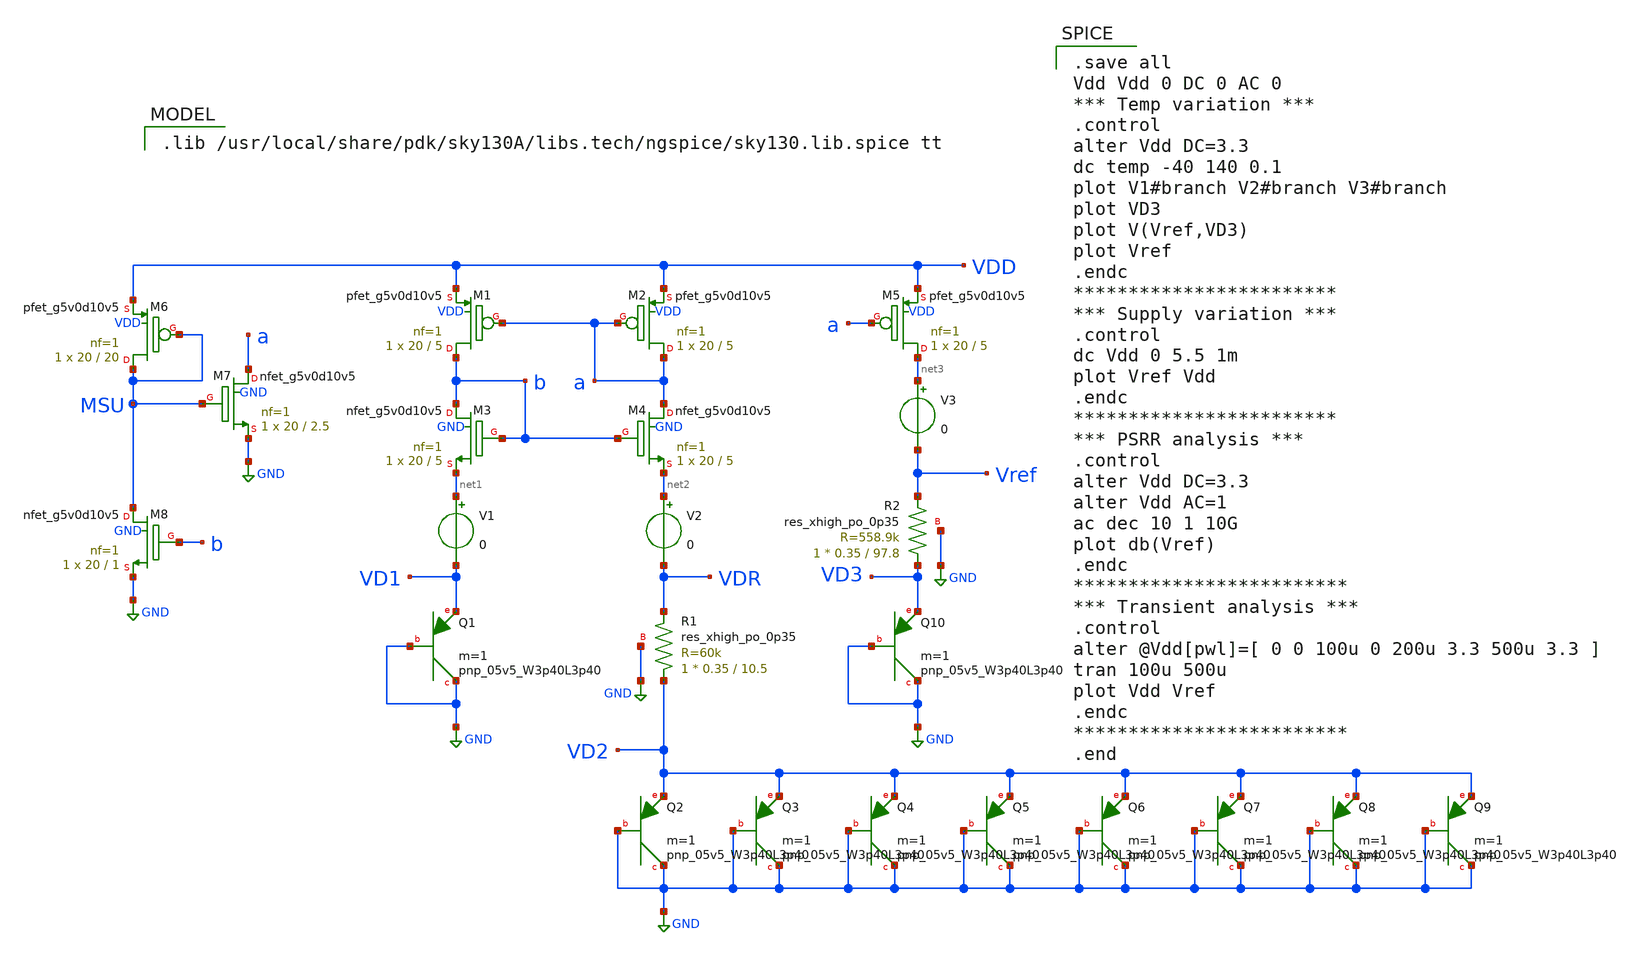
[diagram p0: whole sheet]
** sch_path: 2_BGR_nocas_60k_3p4pnp.sch
**.subckt 2_BGR_nocas_60k_3p4pnp
V1 net1 VD1 0
V2 net2 VDR 0
V3 net3 Vref 0
XR1 VD2 VDR GND sky130_fd_pr__res_xhigh_po_0p35 L=10.5 mult=1 m=1
XR2 VD3 Vref GND sky130_fd_pr__res_xhigh_po_0p35 L=97.8 mult=1 m=1
XM1 b a VDD VDD sky130_fd_pr__pfet_g5v0d10v5 L=5 W=20 nf=1 ad='int((nf+1)/2) * W/nf * 0.29' as='int((nf+2)/2) * W/nf * 0.29'
+ pd='2*int((nf+1)/2) * (W/nf + 0.29)' ps='2*int((nf+2)/2) * (W/nf + 0.29)' nrd='0.29 / W' nrs='0.29 / W'
+ sa=0 sb=0 sd=0 mult=1 m=1
XM2 a a VDD VDD sky130_fd_pr__pfet_g5v0d10v5 L=5 W=20 nf=1 ad='int((nf+1)/2) * W/nf * 0.29' as='int((nf+2)/2) * W/nf * 0.29'
+ pd='2*int((nf+1)/2) * (W/nf + 0.29)' ps='2*int((nf+2)/2) * (W/nf + 0.29)' nrd='0.29 / W' nrs='0.29 / W'
+ sa=0 sb=0 sd=0 mult=1 m=1
XM3 b b net1 GND sky130_fd_pr__nfet_g5v0d10v5 L=5 W=20 nf=1 ad='int((nf+1)/2) * W/nf * 0.29' as='int((nf+2)/2) * W/nf * 0.29'
+ pd='2*int((nf+1)/2) * (W/nf + 0.29)' ps='2*int((nf+2)/2) * (W/nf + 0.29)' nrd='0.29 / W' nrs='0.29 / W'
+ sa=0 sb=0 sd=0 mult=1 m=1
XM4 a b net2 GND sky130_fd_pr__nfet_g5v0d10v5 L=5 W=20 nf=1 ad='int((nf+1)/2) * W/nf * 0.29' as='int((nf+2)/2) * W/nf * 0.29'
+ pd='2*int((nf+1)/2) * (W/nf + 0.29)' ps='2*int((nf+2)/2) * (W/nf + 0.29)' nrd='0.29 / W' nrs='0.29 / W'
+ sa=0 sb=0 sd=0 mult=1 m=1
XM5 net3 a VDD VDD sky130_fd_pr__pfet_g5v0d10v5 L=5 W=20 nf=1 ad='int((nf+1)/2) * W/nf * 0.29' as='int((nf+2)/2) * W/nf * 0.29'
+ pd='2*int((nf+1)/2) * (W/nf + 0.29)' ps='2*int((nf+2)/2) * (W/nf + 0.29)' nrd='0.29 / W' nrs='0.29 / W'
+ sa=0 sb=0 sd=0 mult=1 m=1
XM8 MSU b GND GND sky130_fd_pr__nfet_g5v0d10v5 L=1 W=20 nf=1 ad='int((nf+1)/2) * W/nf * 0.29' as='int((nf+2)/2) * W/nf * 0.29'
+ pd='2*int((nf+1)/2) * (W/nf + 0.29)' ps='2*int((nf+2)/2) * (W/nf + 0.29)' nrd='0.29 / W' nrs='0.29 / W'
+ sa=0 sb=0 sd=0 mult=1 m=1
XM7 a MSU GND GND sky130_fd_pr__nfet_g5v0d10v5 L=2.5 W=20 nf=1 ad='int((nf+1)/2) * W/nf * 0.29' as='int((nf+2)/2) * W/nf * 0.29'
+ pd='2*int((nf+1)/2) * (W/nf + 0.29)' ps='2*int((nf+2)/2) * (W/nf + 0.29)' nrd='0.29 / W' nrs='0.29 / W'
+ sa=0 sb=0 sd=0 mult=1 m=1
XQ1 GND GND VD1 sky130_fd_pr__pnp_05v5_W3p40L3p40 m=1
XQ2 GND GND VD2 sky130_fd_pr__pnp_05v5_W3p40L3p40 m=1
XQ3 GND GND VD2 sky130_fd_pr__pnp_05v5_W3p40L3p40 m=1
XQ4 GND GND VD2 sky130_fd_pr__pnp_05v5_W3p40L3p40 m=1
XQ5 GND GND VD2 sky130_fd_pr__pnp_05v5_W3p40L3p40 m=1
XQ6 GND GND VD2 sky130_fd_pr__pnp_05v5_W3p40L3p40 m=1
XQ7 GND GND VD2 sky130_fd_pr__pnp_05v5_W3p40L3p40 m=1
XQ8 GND GND VD2 sky130_fd_pr__pnp_05v5_W3p40L3p40 m=1
XQ9 GND GND VD2 sky130_fd_pr__pnp_05v5_W3p40L3p40 m=1
XQ10 GND GND VD3 sky130_fd_pr__pnp_05v5_W3p40L3p40 m=1
XM6 MSU MSU VDD VDD sky130_fd_pr__pfet_g5v0d10v5 L=20 W=20 nf=1 ad='int((nf+1)/2) * W/nf * 0.29' as='int((nf+2)/2) * W/nf * 0.29'
+ pd='2*int((nf+1)/2) * (W/nf + 0.29)' ps='2*int((nf+2)/2) * (W/nf + 0.29)' nrd='0.29 / W' nrs='0.29 / W'
+ sa=0 sb=0 sd=0 mult=1 m=1
**** begin user architecture code

.lib /usr/local/share/pdk/sky130A/libs.tech/ngspice/sky130.lib.spice tt


.save all
Vdd Vdd 0 DC 0 AC 0
*** Temp variation ***
.control
alter Vdd DC=3.3
dc temp -40 140 0.1
plot V1#branch V2#branch V3#branch
plot VD3
plot V(Vref,VD3)
plot Vref
.endc
************************
*** Supply variation ***
.control
dc Vdd 0 5.5 1m
plot Vref Vdd
.endc
************************
*** PSRR analysis ***
.control
alter Vdd DC=3.3
alter Vdd AC=1
ac dec 10 1 10G
plot db(Vref)
.endc
*************************
*** Transient analysis ***
.control
alter @Vdd[pwl]=[ 0 0 100u 0 200u 3.3 500u 3.3 ]
tran 100u 500u
plot Vdd Vref
.endc
*************************
.end

**** end user architecture code
**.ends
.GLOBAL GND
.end
